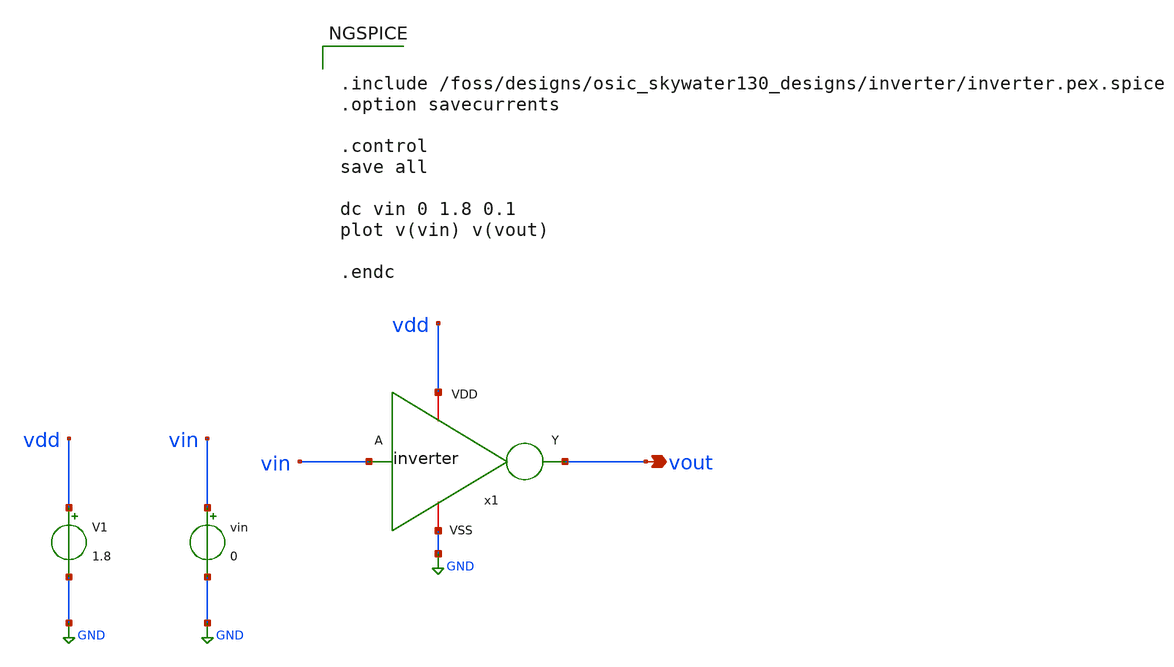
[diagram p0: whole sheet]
** sch_path: inverter/inverter_dc_tb.sch
**.subckt inverter_dc_tb vout
*.opin vout
x1 vdd vin vout GND inverter
V1 vdd GND 1.8
vin vin GND 0
**** begin user architecture code

** opencircuitdesign pdks install
.lib $::SKYWATER_MODELS/sky130.lib.spice tt



.include /foss/designs/osic_skywater130_designs/inverter/inverter.pex.spice
.option savecurrents

.control
save all

dc vin 0 1.8 0.1
plot v(vin) v(vout)

.endc


**** end user architecture code
**.ends
.GLOBAL GND
.end
